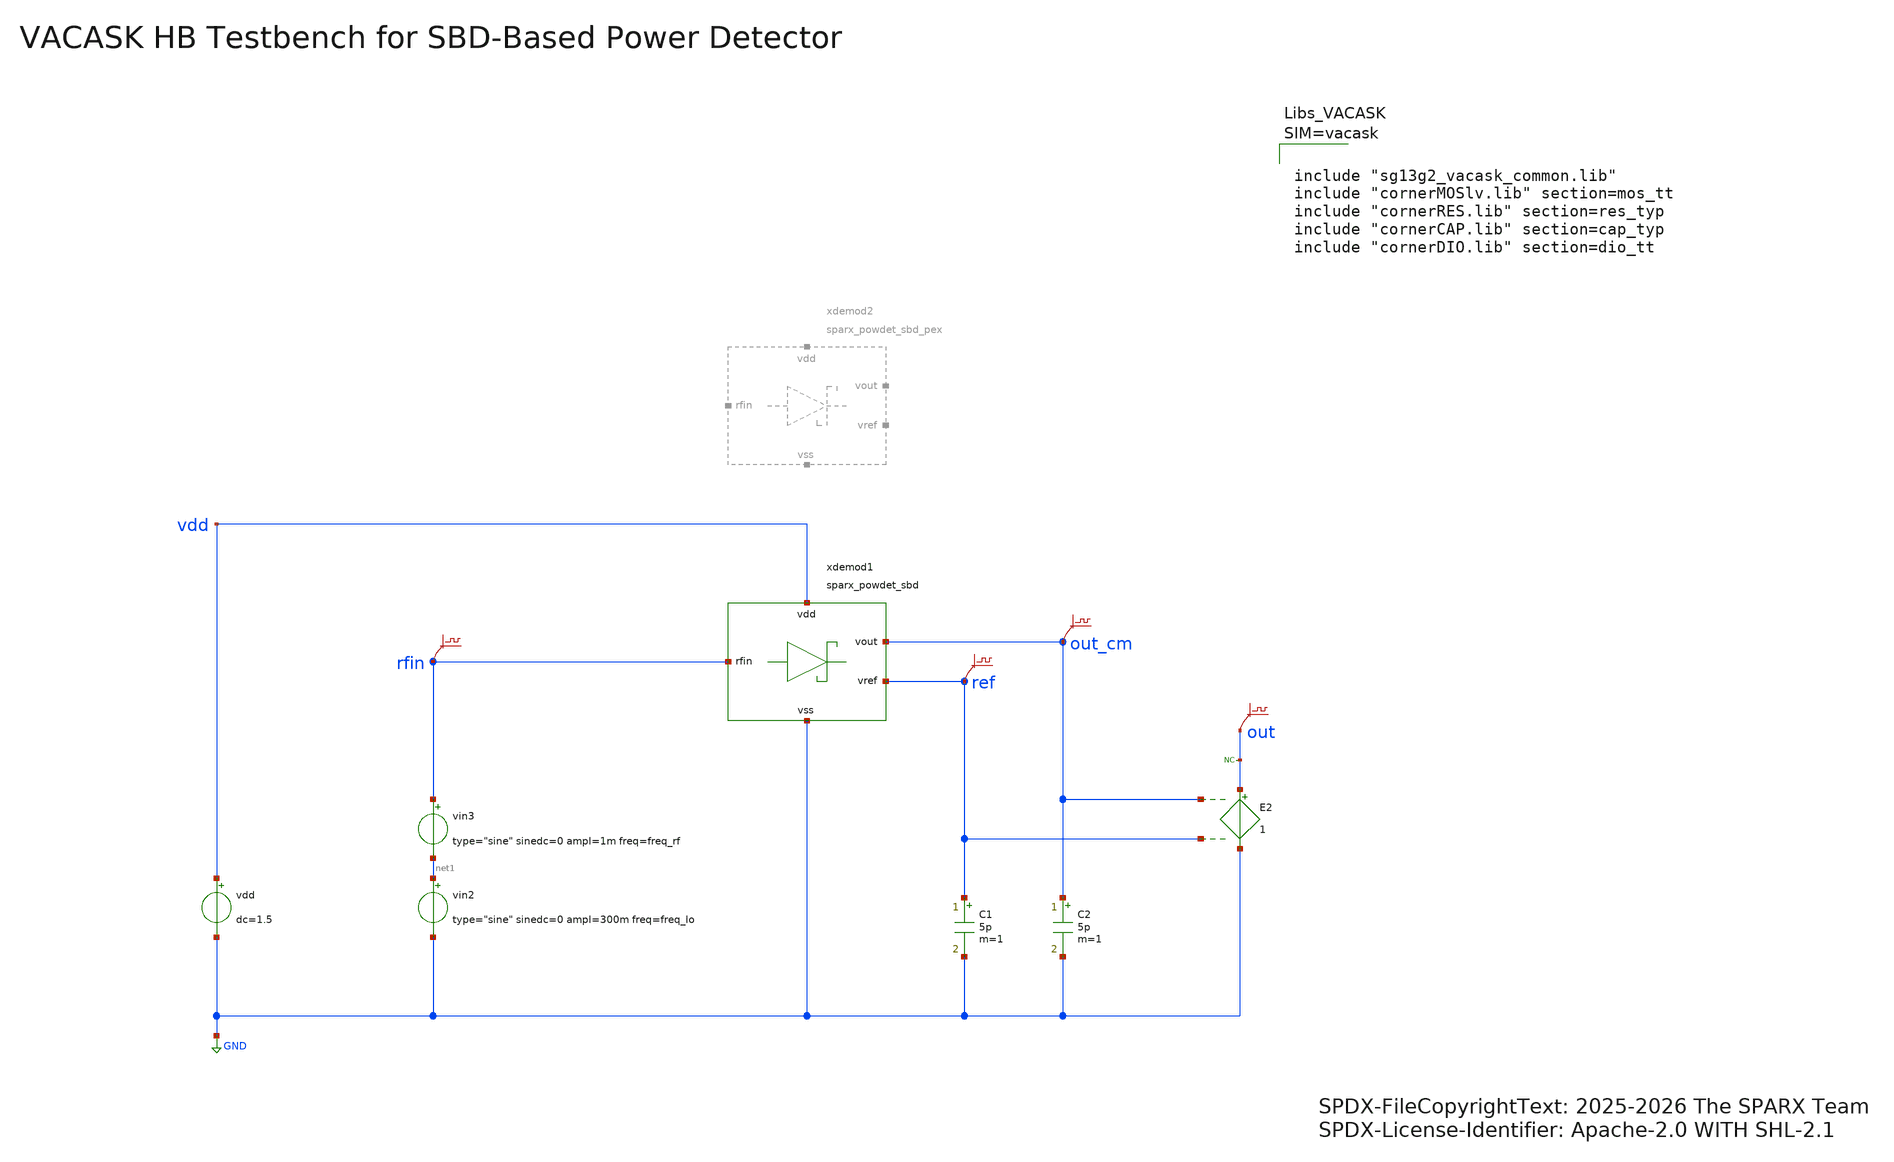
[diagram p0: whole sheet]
** sch_path: testbenches/xschem/sparx_powdet_sbd_tb_hb_vacask.sch
* SPDX-FileCopyrightText: 2025-2026 The SPARX Team
* SPDX-License-Identifier: Apache-2.0 WITH SHL-2.1
* (c) 2026 H. Pretl, ICD@JKU
**.subckt sparx_powdet_sbd_tb_hb_vacask
vdd vdd GND dc=1.5
vin3 rfin net1 type="sine" sinedc=0 ampl=1m freq=freq_rf
vin2 net1 GND type="sine" sinedc=0 ampl=300m freq=freq_lo
xdemod1 out_cm ref vdd rfin GND sparx_powdet_sbd
C1 ref GND 5p m=1
C2 out_cm GND 5p m=1
.save v(rfin)
.save v(out_cm)
.save v(ref)
E2 out GND out_cm ref 1
.save v(out)
* noconn out
**** begin user architecture code






**** end user architecture code
**.ends
.GLOBAL GND
.end
